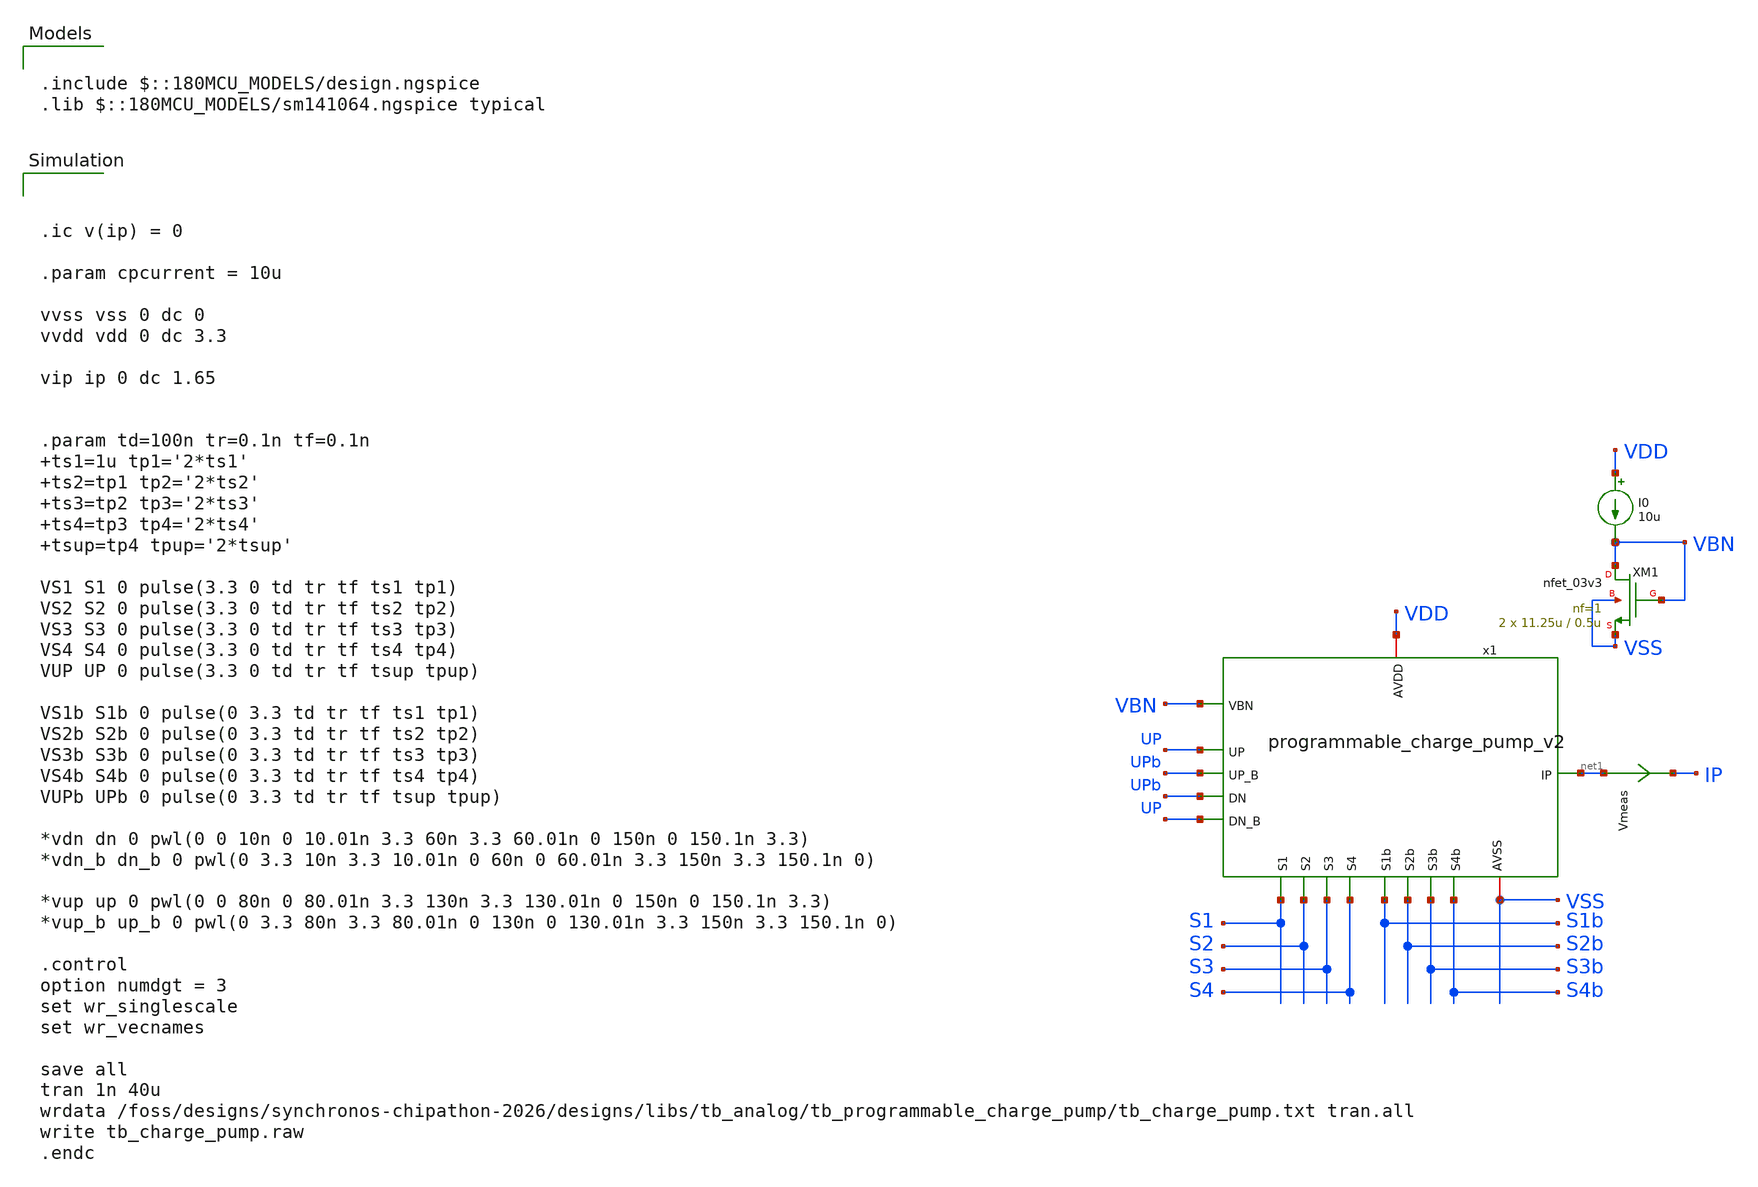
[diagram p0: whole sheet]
** sch_path: designs/libs/tb_analog/tb_programmable_charge_pump/tb_programmable_charge_pump_v2.sch
**.subckt tb_programmable_charge_pump_v2
Vmeas net1 IP 0
.save i(vmeas)
XM1 VBN VBN VSS VSS nfet_03v3 L=0.5u W=11.25u nf=1 ad='int((nf+1)/2) * W/nf * 0.18u' as='int((nf+2)/2) * W/nf * 0.18u'
+ pd='2*int((nf+1)/2) * (W/nf + 0.18u)' ps='2*int((nf+2)/2) * (W/nf + 0.18u)' nrd='0.18u / W' nrs='0.18u / W'
+ sa=0 sb=0 sd=0 m=2
I0 VDD VBN 10u
x1 VSS VDD UP UPb UPb net1 UP VBN S1b S1 S2b S2 S3b S3 S4b S4 programmable_charge_pump_v2
**** begin user architecture code



.ic v(ip) = 0

.param cpcurrent = 10u

vvss vss 0 dc 0
vvdd vdd 0 dc 3.3

vip ip 0 dc 1.65


.param td=100n tr=0.1n tf=0.1n ts1=1u tp1='2*ts1' ts2=tp1 tp2='2*ts2' ts3=tp2 tp3='2*ts3' ts4=tp3 tp4='2*ts4'
+ tsup=tp4 tpup='2*tsup'

VS1 S1 0 pulse(3.3 0 td tr tf ts1 tp1)
VS2 S2 0 pulse(3.3 0 td tr tf ts2 tp2)
VS3 S3 0 pulse(3.3 0 td tr tf ts3 tp3)
VS4 S4 0 pulse(3.3 0 td tr tf ts4 tp4)
VUP UP 0 pulse(3.3 0 td tr tf tsup tpup)

VS1b S1b 0 pulse(0 3.3 td tr tf ts1 tp1)
VS2b S2b 0 pulse(0 3.3 td tr tf ts2 tp2)
VS3b S3b 0 pulse(0 3.3 td tr tf ts3 tp3)
VS4b S4b 0 pulse(0 3.3 td tr tf ts4 tp4)
VUPb UPb 0 pulse(0 3.3 td tr tf tsup tpup)

*vdn dn 0 pwl(0 0 10n 0 10.01n 3.3 60n 3.3 60.01n 0 150n 0 150.1n 3.3)
*vdn_b dn_b 0 pwl(0 3.3 10n 3.3 10.01n 0 60n 0 60.01n 3.3 150n 3.3 150.1n 0)

*vup up 0 pwl(0 0 80n 0 80.01n 3.3 130n 3.3 130.01n 0 150n 0 150.1n 3.3)
*vup_b up_b 0 pwl(0 3.3 80n 3.3 80.01n 0 130n 0 130.01n 3.3 150n 3.3 150.1n 0)

.control
option numdgt = 3
set wr_singlescale
set wr_vecnames

save all
tran 1n 40u
wrdata
+ /foss/designs/synchronos-chipathon-2026/designs/libs/tb_analog/tb_programmable_charge_pump/tb_charge_pump.txt tran.all
write tb_charge_pump.raw
.endc



.include $::180MCU_MODELS/design.ngspice
.lib $::180MCU_MODELS/sm141064.ngspice typical

**** end user architecture code
**.ends
.end
